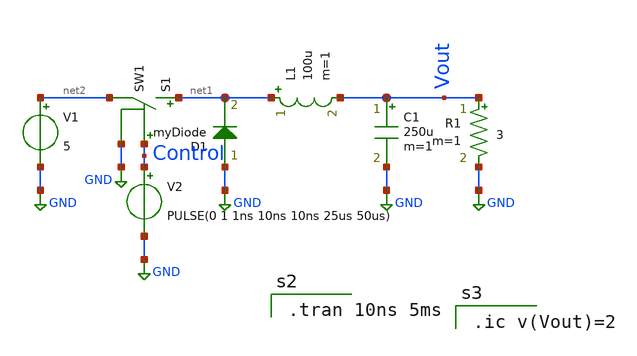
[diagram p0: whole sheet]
** sch_path: Xschem/buck_conv.sch
**.subckt buck_conv
S1 net1 net2 Control GND SW1
C1 Vout GND 250u m=1
R1 Vout GND 3 m=1
L1 net1 Vout 100u m=1
D1 GND net1 myDiode area=1
V1 net2 GND 5
V2 Control GND PULSE(0 1 1ns 10ns 10ns 25us 50us)
**** begin user architecture code

.tran 10ns 5ms


.model myDiode D (IS=2.52n N=1.752 RS=0.568 CJO=4p BV=100 IBV=0.1p TT=4n)


.ic v(Vout)=2

**** end user architecture code
**.ends
.GLOBAL GND
**** begin user architecture code
.MODEL SW1 SW( VT=0.9 VH=0.01 RON=0.01 ROFF=10G )
**** end user architecture code
.end
